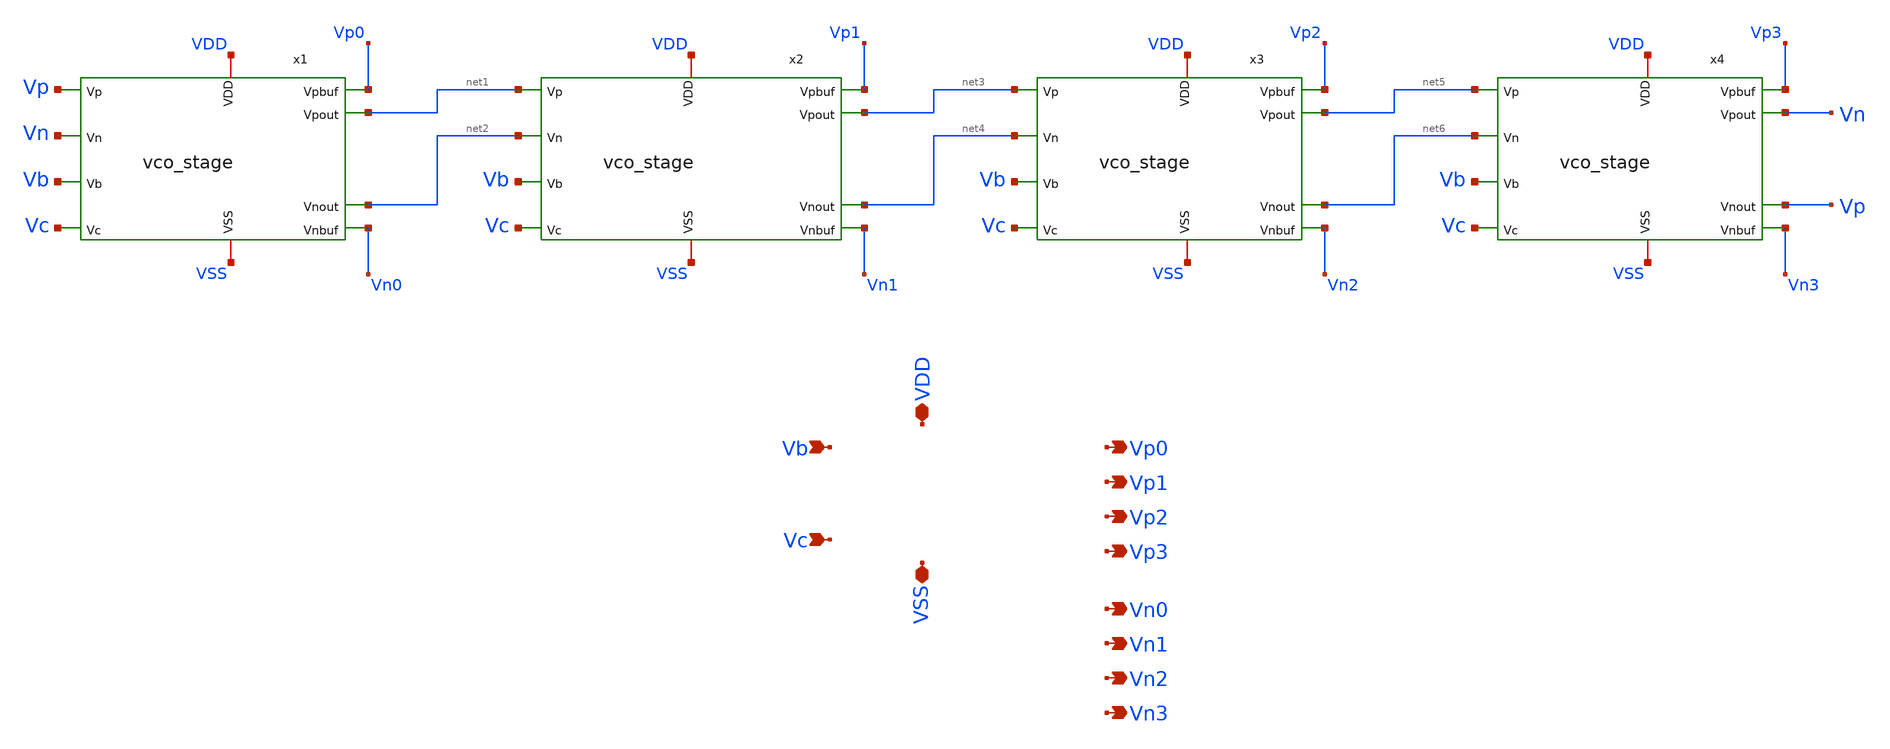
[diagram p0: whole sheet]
** sch_path: xschem/vco_core.sch
**.subckt vco_core VDD VSS Vb Vc Vp0 Vp1 Vp2 Vp3 Vn0 Vn1 Vn2 Vn3
*.iopin VDD
*.iopin VSS
*.ipin Vb
*.ipin Vc
*.opin Vp0
*.opin Vp1
*.opin Vp2
*.opin Vp3
*.opin Vn0
*.opin Vn1
*.opin Vn2
*.opin Vn3
x1 VDD VSS Vp Vn Vb Vc net1 net2 Vp0 Vn0 vco_stage
x2 VDD VSS net1 net2 Vb Vc net3 net4 Vp1 Vn1 vco_stage
x3 VDD VSS net3 net4 Vb Vc net5 net6 Vp2 Vn2 vco_stage
x4 VDD VSS net5 net6 Vb Vc Vn Vp Vp3 Vn3 vco_stage
**.ends
.end
